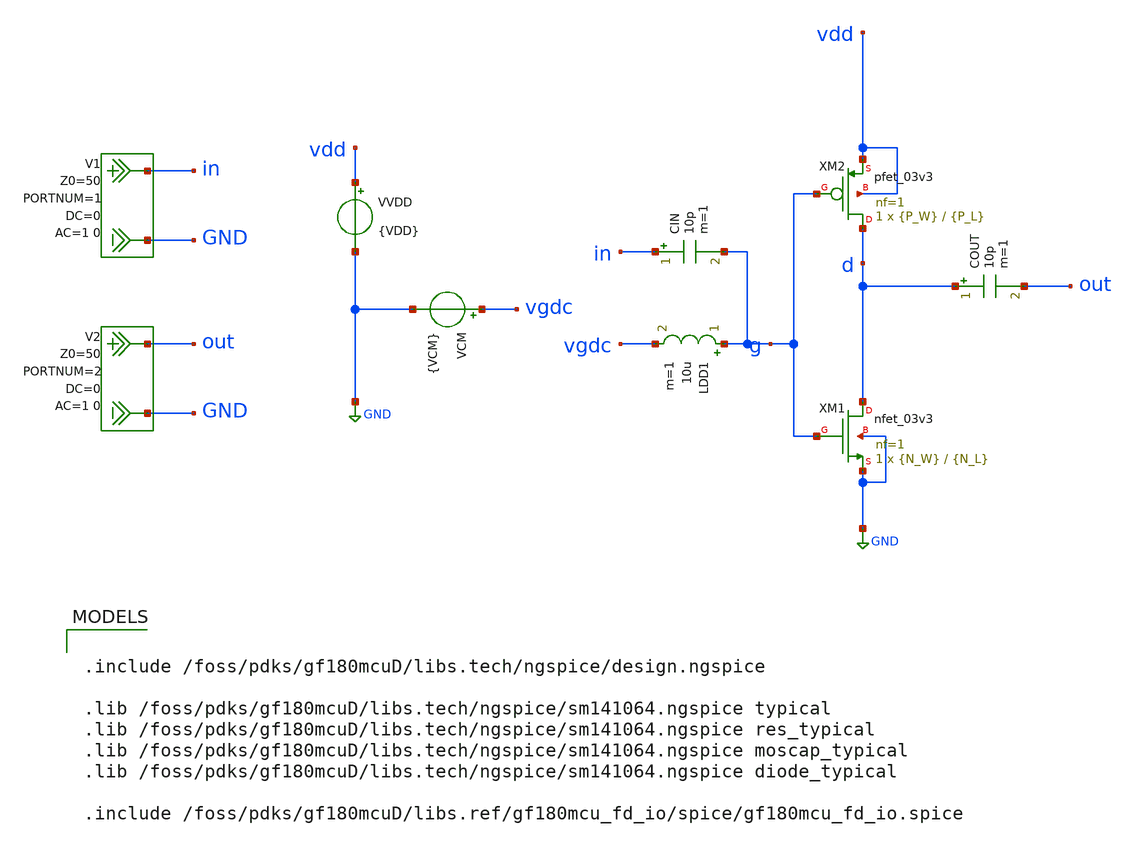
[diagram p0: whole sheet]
** sch_path: NFmin_Simulation/simulations/03_cmos/nfmin_jd_cmos_inv.sch
**.subckt nfmin_jd_cmos_inv
VCM vgdc GND {VCM}
VVDD vdd GND {VDD}
COUT d out 10p m=1
CIN in g 10p m=1
XM2 d g vdd vdd pfet_03v3 L={P_L} W={P_W} nf=1 ad='int((nf+1)/2) * W/nf * 0.18u' as='int((nf+2)/2) * W/nf * 0.18u'
+ pd='2*int((nf+1)/2) * (W/nf + 0.18u)' ps='2*int((nf+2)/2) * (W/nf + 0.18u)' nrd='0.18u / W' nrs='0.18u / W'
+ sa=0 sb=0 sd=0 m=1
XM1 d g GND GND nfet_03v3 L={N_L} W={N_W} nf=1 ad='int((nf+1)/2) * W/nf * 0.18u' as='int((nf+2)/2) * W/nf * 0.18u'
+ pd='2*int((nf+1)/2) * (W/nf + 0.18u)' ps='2*int((nf+2)/2) * (W/nf + 0.18u)' nrd='0.18u / W' nrs='0.18u / W'
+ sa=0 sb=0 sd=0 m=1
V1 in GND DC 0 AC 1 0 portnum 1 z0 50
V2 out GND DC 0 AC 1 0 portnum 2 z0 50
LDD1 g vgdc 10u m=1
**** begin user architecture code

.include /foss/pdks/gf180mcuD/libs.tech/ngspice/design.ngspice

.lib /foss/pdks/gf180mcuD/libs.tech/ngspice/sm141064.ngspice typical
.lib /foss/pdks/gf180mcuD/libs.tech/ngspice/sm141064.ngspice res_typical
.lib /foss/pdks/gf180mcuD/libs.tech/ngspice/sm141064.ngspice moscap_typical
.lib /foss/pdks/gf180mcuD/libs.tech/ngspice/sm141064.ngspice diode_typical

.include /foss/pdks/gf180mcuD/libs.ref/gf180mcu_fd_io/spice/gf180mcu_fd_io.spice



.option savecurrents

.param fnoicor=0
.param sw_stat_mismatch=0

.param VDD=1.8
.param VCM=0.9

* Default geometry values
.param N_W=0.22e-6
.param N_L=0.28e-6
.param P_W=0.66e-6
.param P_L=0.28e-6

.control
  set noaskquit
  save all

  echo N_W_m N_L_m P_W_m P_L_m VCM ID_A JD_N_mA_per_um JD_P_mA_per_um VOUT_DC > inv_geom_jd.txt
  echo N_W_m N_L_m P_W_m P_L_m VCM NFmin_dB NF_dB Rn SOpt_real SOpt_imag > inv_geom_nf.txt

  * NMOS width sweep
  foreach nwval 0.22e-6 1e-6 5e-6 10e-6

    * NMOS length sweep
    foreach nlval 0.28e-6 0.36e-6 0.50e-6

      * PMOS width sweep
      foreach pwval 0.66e-6 2e-6 10e-6 20e-6 30e-6

        * PMOS length sweep
        foreach plval 0.28e-6 0.36e-6 0.50e-6

          * Common gate bias sweep
          foreach vcm 0.55 0.60 0.65 0.70 0.75 0.80 0.85 0.90 0.95 1.00 1.05 1.10 1.15

            alterparam N_W = $nwval
            alterparam N_L = $nlval
            alterparam P_W = $pwval
            alterparam P_L = $plval
            alterparam VCM = $vcm
            reset

            op

            let id_inv = abs(i(vvdd))
            let jd_n = 1e-3*id_inv/$nwval
            let jd_p = 1e-3*id_inv/$pwval
            let vout_dc = v(d)

            echo $nwval $nlval $pwval $plval $vcm $&id_inv $&jd_n $&jd_p $&vout_dc >>
+ inv_geom_jd.txt

            sp lin 1 2.4e9 2.4e9 1

            let nfmin_val = real(NFmin)
            let nf_val = real(NF)
            let rn_val = real(Rn)
            let sopt_re = real(SOpt)
            let sopt_im = imag(SOpt)

            echo $nwval $nlval $pwval $plval $vcm $&nfmin_val $&nf_val $&rn_val $&sopt_re $&sopt_im
+ >> inv_geom_nf.txt

          end

        end

      end

    end

  end

.endc



**** end user architecture code
**.ends
.GLOBAL GND
.end
